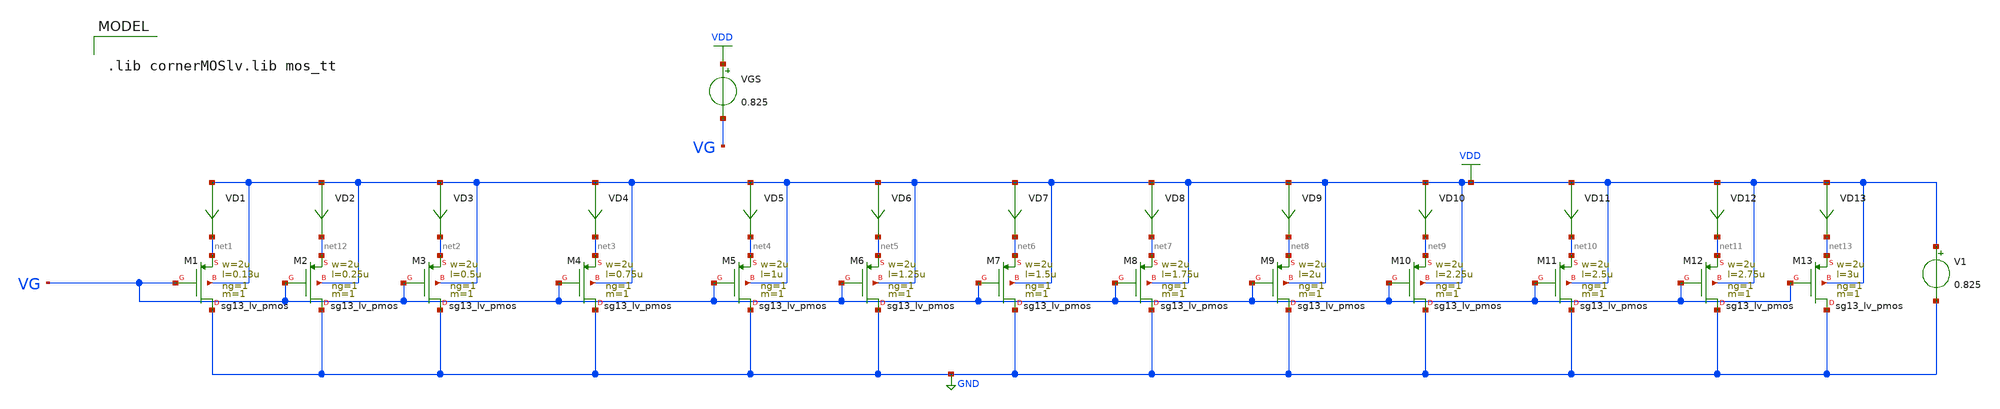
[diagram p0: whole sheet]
** sch_path: Design-Files/gmid_pmos_sg13_lv_pmos_tb.sch
**.subckt gmid_pmos_sg13_lv_pmos_tb
V1 VDD GND 0.825
VGS VDD VG 0.825
VD1 VDD net1 0
.save i(vd1)
VD2 VDD net12 0
.save i(vd2)
VD3 VDD net2 0
.save i(vd3)
VD4 VDD net3 0
.save i(vd4)
VD5 VDD net4 0
.save i(vd5)
VD6 VDD net5 0
.save i(vd6)
VD7 VDD net6 0
.save i(vd7)
VD8 VDD net7 0
.save i(vd8)
VD9 VDD net8 0
.save i(vd9)
VD10 VDD net9 0
.save i(vd10)
VD11 VDD net10 0
.save i(vd11)
XM1 GND VG net1 VDD sg13_lv_pmos w=2u l=0.13u ng=1 m=1 mm_ok=1
XM2 GND VG net12 VDD sg13_lv_pmos w=2u l=0.25u ng=1 m=1 mm_ok=1
XM3 GND VG net2 VDD sg13_lv_pmos w=2u l=0.5u ng=1 m=1 mm_ok=1
XM4 GND VG net3 VDD sg13_lv_pmos w=2u l=0.75u ng=1 m=1 mm_ok=1
XM5 GND VG net4 VDD sg13_lv_pmos w=2u l=1u ng=1 m=1 mm_ok=1
XM6 GND VG net5 VDD sg13_lv_pmos w=2u l=1.25u ng=1 m=1 mm_ok=1
XM7 GND VG net6 VDD sg13_lv_pmos w=2u l=1.5u ng=1 m=1 mm_ok=1
XM8 GND VG net7 VDD sg13_lv_pmos w=2u l=1.75u ng=1 m=1 mm_ok=1
XM9 GND VG net8 VDD sg13_lv_pmos w=2u l=2u ng=1 m=1 mm_ok=1
XM10 GND VG net9 VDD sg13_lv_pmos w=2u l=2.25u ng=1 m=1 mm_ok=1
XM11 GND VG net10 VDD sg13_lv_pmos w=2u l=2.5u ng=1 m=1 mm_ok=1
XM12 GND VG net11 VDD sg13_lv_pmos w=2u l=2.75u ng=1 m=1 mm_ok=1
VD12 VDD net11 0
.save i(vd12)
XM13 GND VG net13 VDD sg13_lv_pmos w=2u l=3u ng=1 m=1 mm_ok=1
VD13 VDD net13 0
.save i(vd13)
**** begin user architecture code


.save @n.xm1.nsg13_lv_pmos[gm]
.save @n.xm1.nsg13_lv_pmos[id]
.save @n.xm1.nsg13_lv_pmos[vth]
.save @n.xm1.nsg13_lv_pmos[gds]
.save @n.xm1.nsg13_lv_pmos[cgg]
.save @n.xm1.nsg13_lv_pmos[cgs]
.save @n.xm1.nsg13_lv_pmos[cgd]
.save @n.xm2.nsg13_lv_pmos[gm]
.save @n.xm2.nsg13_lv_pmos[id]
.save @n.xm2.nsg13_lv_pmos[vth]
.save @n.xm2.nsg13_lv_pmos[gds]
.save @n.xm2.nsg13_lv_pmos[cgg]
.save @n.xm2.nsg13_lv_pmos[cgs]
.save @n.xm2.nsg13_lv_pmos[cgd]
.save @n.xm3.nsg13_lv_pmos[gm]
.save @n.xm3.nsg13_lv_pmos[id]
.save @n.xm3.nsg13_lv_pmos[vth]
.save @n.xm3.nsg13_lv_pmos[gds]
.save @n.xm3.nsg13_lv_pmos[cgg]
.save @n.xm3.nsg13_lv_pmos[cgs]
.save @n.xm3.nsg13_lv_pmos[cgd]
.save @n.xm4.nsg13_lv_pmos[gm]
.save @n.xm4.nsg13_lv_pmos[id]
.save @n.xm4.nsg13_lv_pmos[vth]
.save @n.xm4.nsg13_lv_pmos[gds]
.save @n.xm4.nsg13_lv_pmos[cgg]
.save @n.xm4.nsg13_lv_pmos[cgs]
.save @n.xm4.nsg13_lv_pmos[cgd]
.save @n.xm5.nsg13_lv_pmos[gm]
.save @n.xm5.nsg13_lv_pmos[id]
.save @n.xm5.nsg13_lv_pmos[vth]
.save @n.xm5.nsg13_lv_pmos[gds]
.save @n.xm5.nsg13_lv_pmos[cgg]
.save @n.xm5.nsg13_lv_pmos[cgs]
.save @n.xm5.nsg13_lv_pmos[cgd]
.save @n.xm6.nsg13_lv_pmos[gm]
.save @n.xm6.nsg13_lv_pmos[id]
.save @n.xm6.nsg13_lv_pmos[vth]
.save @n.xm6.nsg13_lv_pmos[gds]
.save @n.xm6.nsg13_lv_pmos[cgg]
.save @n.xm6.nsg13_lv_pmos[cgs]
.save @n.xm6.nsg13_lv_pmos[cgd]
.save @n.xm7.nsg13_lv_pmos[gm]
.save @n.xm7.nsg13_lv_pmos[id]
.save @n.xm7.nsg13_lv_pmos[vth]
.save @n.xm7.nsg13_lv_pmos[gds]
.save @n.xm7.nsg13_lv_pmos[cgg]
.save @n.xm7.nsg13_lv_pmos[cgs]
.save @n.xm7.nsg13_lv_pmos[cgd]
.save @n.xm7.nsg13_lv_pmos[gm]
.save @n.xm7.nsg13_lv_pmos[id]
.save @n.xm7.nsg13_lv_pmos[vth]
.save @n.xm7.nsg13_lv_pmos[gds]
.save @n.xm7.nsg13_lv_pmos[cgg]
.save @n.xm7.nsg13_lv_pmos[cgs]
.save @n.xm7.nsg13_lv_pmos[cgd]
.save @n.xm8.nsg13_lv_pmos[gm]
.save @n.xm8.nsg13_lv_pmos[id]
.save @n.xm8.nsg13_lv_pmos[vth]
.save @n.xm8.nsg13_lv_pmos[gds]
.save @n.xm8.nsg13_lv_pmos[cgg]
.save @n.xm8.nsg13_lv_pmos[cgs]
.save @n.xm8.nsg13_lv_pmos[cgd]
.save @n.xm9.nsg13_lv_pmos[gm]
.save @n.xm9.nsg13_lv_pmos[id]
.save @n.xm9.nsg13_lv_pmos[vth]
.save @n.xm9.nsg13_lv_pmos[gds]
.save @n.xm9.nsg13_lv_pmos[cgg]
.save @n.xm9.nsg13_lv_pmos[cgs]
.save @n.xm9.nsg13_lv_pmos[cgd]
.save @n.xm10.nsg13_lv_pmos[gm]
.save @n.xm10.nsg13_lv_pmos[id]
.save @n.xm10.nsg13_lv_pmos[vth]
.save @n.xm10.nsg13_lv_pmos[gds]
.save @n.xm10.nsg13_lv_pmos[cgg]
.save @n.xm10.nsg13_lv_pmos[cgs]
.save @n.xm10.nsg13_lv_pmos[cgd]
.save @n.xm11.nsg13_lv_pmos[gm]
.save @n.xm11.nsg13_lv_pmos[id]
.save @n.xm11.nsg13_lv_pmos[vth]
.save @n.xm11.nsg13_lv_pmos[gds]
.save @n.xm11.nsg13_lv_pmos[cgg]
.save @n.xm11.nsg13_lv_pmos[cgs]
.save @n.xm11.nsg13_lv_pmos[cgd]
.save @n.xm12.nsg13_lv_pmos[gm]
.save @n.xm12.nsg13_lv_pmos[id]
.save @n.xm12.nsg13_lv_pmos[vth]
.save @n.xm12.nsg13_lv_pmos[gds]
.save @n.xm12.nsg13_lv_pmos[cgg]
.save @n.xm12.nsg13_lv_pmos[cgs]
.save @n.xm12.nsg13_lv_pmos[cgd]
.save @n.xm13.nsg13_lv_pmos[gm]
.save @n.xm13.nsg13_lv_pmos[id]
.save @n.xm13.nsg13_lv_pmos[vth]
.save @n.xm13.nsg13_lv_pmos[gds]
.save @n.xm13.nsg13_lv_pmos[cgg]
.save @n.xm13.nsg13_lv_pmos[cgs]
.save @n.xm13.nsg13_lv_pmos[cgd]




.option wnflag=1
.option savecurrents
.temp 27
.control
save all
dc VGS 0.01 1.65 0.1m
remzerovec
write /foss/designs/IHP130_Designs/PDK_CHAR/LV_PMOS/gmid_pmos_sg13_lv_pmos_tb.raw

plot @n.xm1.nsg13_lv_pmos[gm]
plot @n.xm2.nsg13_lv_pmos[gm]
plot @n.xm3.nsg13_lv_pmos[gm]
plot @n.xm4.nsg13_lv_pmos[gm]
plot @n.xm5.nsg13_lv_pmos[gm]
plot @n.xm6.nsg13_lv_pmos[gm]
plot @n.xm7.nsg13_lv_pmos[gm]
plot @n.xm8.nsg13_lv_pmos[gm]
plot @n.xm9.nsg13_lv_pmos[gm]
plot @n.xm10.nsg13_lv_pmos[gm]
plot @n.xm11.nsg13_lv_pmos[gm]
plot @n.xm12.nsg13_lv_pmos[gm]
plot @n.xm13.nsg13_lv_pmos[gm]
plot @n.xm1.nsg13_lv_pmos[vth]
plot @n.xm1.nsg13_lv_pmos[ids]
let gm1=@n.xm1.nsg1_lv_pmos[gm]
let id1=@n.xm1.nsg1_lv_pmos[ids]
let gmid1=gm1/id1
plot gmid1

wrdata /foss/designs/IHP130_Designs/PDK_CHAR/LV_PMOS/gmid_pmos_1_sg13_lv_pmos_tb.txt
+ @n.xm1.nsg13_lv_pmos[gm] i(VD1) @n.xm1.nsg13_lv_pmos[vth] @n.xm1.nsg13_lv_pmos[gds] @n.xm1.nsg13_lv_pmos[cgg]
+ @n.xm1.nsg13_lv_pmos[cgs] @n.xm1.nsg13_lv_pmos[cgd]
wrdata /foss/designs/IHP130_Designs/PDK_CHAR/LV_PMOS/gmid_pmos_2_sg13_lv_pmos_tb.txt
+ @n.xm2.nsg13_lv_pmos[gm] i(VD2) @n.xm2.nsg13_lv_pmos[vth] @n.xm2.nsg13_lv_pmos[gds] @n.xm2.nsg13_lv_pmos[cgg]
+ @n.xm2.nsg13_lv_pmos[cgs] @n.xm2.nsg13_lv_pmos[cgd]
wrdata /foss/designs/IHP130_Designs/PDK_CHAR/LV_PMOS/gmid_pmos_3_sg13_lv_pmos_tb.txt
+ @n.xm3.nsg13_lv_pmos[gm] i(VD3) @n.xm3.nsg13_lv_pmos[vth] @n.xm3.nsg13_lv_pmos[gds] @n.xm3.nsg13_lv_pmos[cgg]
+ @n.xm3.nsg13_lv_pmos[cgs] @n.xm3.nsg13_lv_pmos[cgd]
wrdata /foss/designs/IHP130_Designs/PDK_CHAR/LV_PMOS/gmid_pmos_4_sg13_lv_pmos_tb.txt
+ @n.xm4.nsg13_lv_pmos[gm] i(VD4) @n.xm4.nsg13_lv_pmos[vth] @n.xm4.nsg13_lv_pmos[gds] @n.xm4.nsg13_lv_pmos[cgg]
+ @n.xm4.nsg13_lv_pmos[cgs] @n.xm4.nsg13_lv_pmos[cgd]
wrdata /foss/designs/IHP130_Designs/PDK_CHAR/LV_PMOS/gmid_pmos_5_sg13_lv_pmos_tb.txt
+ @n.xm5.nsg13_lv_pmos[gm] i(VD5) @n.xm5.nsg13_lv_pmos[vth] @n.xm5.nsg13_lv_pmos[gds] @n.xm5.nsg13_lv_pmos[cgg]
+ @n.xm5.nsg13_lv_pmos[cgs] @n.xm5.nsg13_lv_pmos[cgd]
wrdata /foss/designs/IHP130_Designs/PDK_CHAR/LV_PMOS/gmid_pmos_6_sg13_lv_pmos_tb.txt
+ @n.xm6.nsg13_lv_pmos[gm] i(VD6) @n.xm6.nsg13_lv_pmos[vth] @n.xm6.nsg13_lv_pmos[gds] @n.xm6.nsg13_lv_pmos[cgg]
+ @n.xm6.nsg13_lv_pmos[cgs] @n.xm6.nsg13_lv_pmos[cgd]
wrdata /foss/designs/IHP130_Designs/PDK_CHAR/LV_PMOS/gmid_pmos_7_sg13_lv_pmos_tb.txt
+ @n.xm7.nsg13_lv_pmos[gm] i(VD7) @n.xm7.nsg13_lv_pmos[vth] @n.xm7.nsg13_lv_pmos[gds] @n.xm7.nsg13_lv_pmos[cgg]
+ @n.xm7.nsg13_lv_pmos[cgs] @n.xm7.nsg13_lv_pmos[cgd]
wrdata /foss/designs/IHP130_Designs/PDK_CHAR/LV_PMOS/gmid_pmos_8_sg13_lv_pmos_tb.txt
+ @n.xm8.nsg13_lv_pmos[gm] i(VD8) @n.xm8.nsg13_lv_pmos[vth] @n.xm8.nsg13_lv_pmos[gds] @n.xm8.nsg13_lv_pmos[cgg]
+ @n.xm8.nsg13_lv_pmos[cgs] @n.xm8.nsg13_lv_pmos[cgd]
wrdata /foss/designs/IHP130_Designs/PDK_CHAR/LV_PMOS/gmid_pmos_9_sg13_lv_pmos_tb.txt
+ @n.xm9.nsg13_lv_pmos[gm] i(VD9) @n.xm9.nsg13_lv_pmos[vth] @n.xm9.nsg13_lv_pmos[gds] @n.xm9.nsg13_lv_pmos[cgg]
+ @n.xm9.nsg13_lv_pmos[cgs] @n.xm9.nsg13_lv_pmos[cgd]
wrdata /foss/designs/IHP130_Designs/PDK_CHAR/LV_PMOS/gmid_pmos_10_sg13_lv_pmos_tb.txt
+ @n.xm10.nsg13_lv_pmos[gm] i(VD10) @n.xm10.nsg13_lv_pmos[vth] @n.xm10.nsg13_lv_pmos[gds] @n.xm10.nsg13_lv_pmos[cgg]
+ @n.xm10.nsg13_lv_pmos[cgs] @n.xm10.nsg13_lv_pmos[cgd]
wrdata /foss/designs/IHP130_Designs/PDK_CHAR/LV_PMOS/gmid_pmos_11_sg13_lv_pmos_tb.txt
+ @n.xm11.nsg13_lv_pmos[gm] i(VD11) @n.xm11.nsg13_lv_pmos[vth] @n.xm11.nsg13_lv_pmos[gds] @n.xm11.nsg13_lv_pmos[cgg]
+ @n.xm11.nsg13_lv_pmos[cgs] @n.xm11.nsg13_lv_pmos[cgd]
wrdata /foss/designs/IHP130_Designs/PDK_CHAR/LV_PMOS/gmid_pmos_12_sg13_lv_pmos_tb.txt
+ @n.xm12.nsg13_lv_pmos[gm] i(VD12) @n.xm12.nsg13_lv_pmos[vth] @n.xm12.nsg13_lv_pmos[gds] @n.xm12.nsg13_lv_pmos[cgg]
+ @n.xm12.nsg13_lv_pmos[cgs] @n.xm12.nsg13_lv_pmos[cgd]
wrdata /foss/designs/IHP130_Designs/PDK_CHAR/LV_PMOS/gmid_pmos_13_sg13_lv_pmos_tb.txt
+ @n.xm13.nsg13_lv_pmos[gm] i(VD13) @n.xm13.nsg13_lv_pmos[vth] @n.xm13.nsg13_lv_pmos[gds] @n.xm12.nsg13_lv_pmos[cgg]
+ @n.xm13.nsg13_lv_pmos[cgs] @n.xm13.nsg13_lv_pmos[cgd]
set appendwrite
op
remzerovec
write /foss/designs/IHP130_Designs/PDK_CHAR/LV_PMOS/gmid_pmos_sg13_lv_pmos_tb.raw
*quit 0
.endc



.lib cornerMOSlv.lib mos_tt

**** end user architecture code
**.ends
.GLOBAL GND
.GLOBAL VDD
.end
